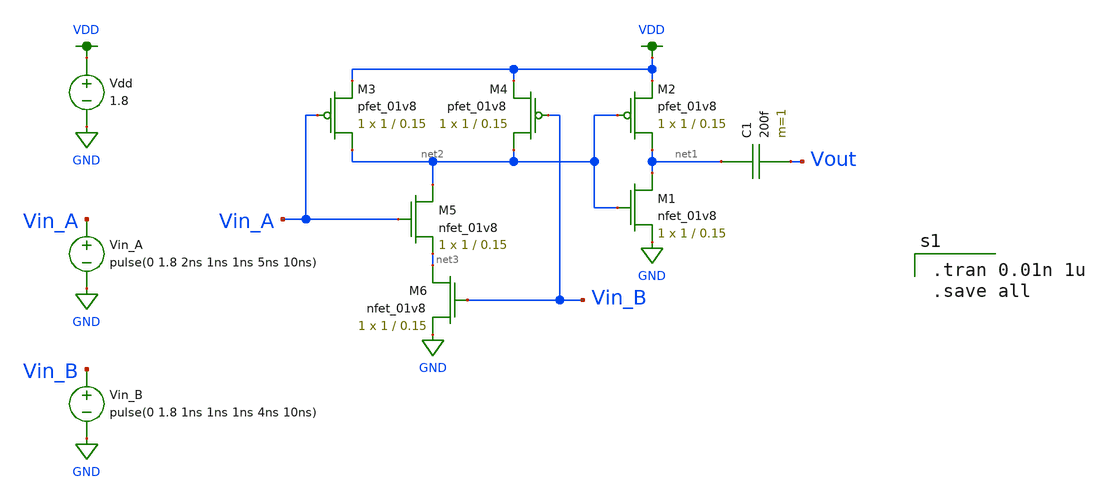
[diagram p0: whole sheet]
** sch_path: MP1/xschem/AND_tran.sch
**.subckt AND_tran
XM1 net1 net2 GND GND sky130_fd_pr__nfet_01v8 L=0.15 W=1 nf=1 ad='int((nf+1)/2) * W/nf * 0.29' as='int((nf+2)/2) * W/nf * 0.29'
+ pd='2*int((nf+1)/2) * (W/nf + 0.29)' ps='2*int((nf+2)/2) * (W/nf + 0.29)' nrd='0.29 / W' nrs='0.29 / W'
+ sa=0 sb=0 sd=0 mult=1 m=1
XM2 net1 net2 VDD VDD sky130_fd_pr__pfet_01v8 L=0.15 W=1 nf=1 ad='int((nf+1)/2) * W/nf * 0.29' as='int((nf+2)/2) * W/nf * 0.29'
+ pd='2*int((nf+1)/2) * (W/nf + 0.29)' ps='2*int((nf+2)/2) * (W/nf + 0.29)' nrd='0.29 / W' nrs='0.29 / W'
+ sa=0 sb=0 sd=0 mult=1 m=1
Vdd VDD GND 1.8
Vin_A Vin_A GND pulse(0 1.8 2ns 1ns 1ns 5ns 10ns)
XM3 net2 Vin_A VDD VDD sky130_fd_pr__pfet_01v8 L=0.15 W=1 nf=1 ad='int((nf+1)/2) * W/nf * 0.29' as='int((nf+2)/2) * W/nf * 0.29'
+ pd='2*int((nf+1)/2) * (W/nf + 0.29)' ps='2*int((nf+2)/2) * (W/nf + 0.29)' nrd='0.29 / W' nrs='0.29 / W'
+ sa=0 sb=0 sd=0 mult=1 m=1
XM4 net2 Vin_B VDD VDD sky130_fd_pr__pfet_01v8 L=0.15 W=1 nf=1 ad='int((nf+1)/2) * W/nf * 0.29' as='int((nf+2)/2) * W/nf * 0.29'
+ pd='2*int((nf+1)/2) * (W/nf + 0.29)' ps='2*int((nf+2)/2) * (W/nf + 0.29)' nrd='0.29 / W' nrs='0.29 / W'
+ sa=0 sb=0 sd=0 mult=1 m=1
XM5 net2 Vin_A net3 GND sky130_fd_pr__nfet_01v8 L=0.15 W=1 nf=1 ad='int((nf+1)/2) * W/nf * 0.29' as='int((nf+2)/2) * W/nf * 0.29'
+ pd='2*int((nf+1)/2) * (W/nf + 0.29)' ps='2*int((nf+2)/2) * (W/nf + 0.29)' nrd='0.29 / W' nrs='0.29 / W'
+ sa=0 sb=0 sd=0 mult=1 m=1
XM6 net3 Vin_B GND GND sky130_fd_pr__nfet_01v8 L=0.15 W=1 nf=1 ad='int((nf+1)/2) * W/nf * 0.29' as='int((nf+2)/2) * W/nf * 0.29'
+ pd='2*int((nf+1)/2) * (W/nf + 0.29)' ps='2*int((nf+2)/2) * (W/nf + 0.29)' nrd='0.29 / W' nrs='0.29 / W'
+ sa=0 sb=0 sd=0 mult=1 m=1
Vin_B Vin_B GND pulse(0 1.8 1ns 1ns 1ns 4ns 10ns)
C1 net1 Vout 200f m=1
**** begin user architecture code

.option wnflag=1
.lib ~/skywater/skywater-pdk/libraries/sky130_fd_pr_ngspice/latest/models/sky130.lib.spice tt


.tran 0.01n 1u
.save all

**** end user architecture code
**.ends
.GLOBAL VDD
.GLOBAL GND
.end
